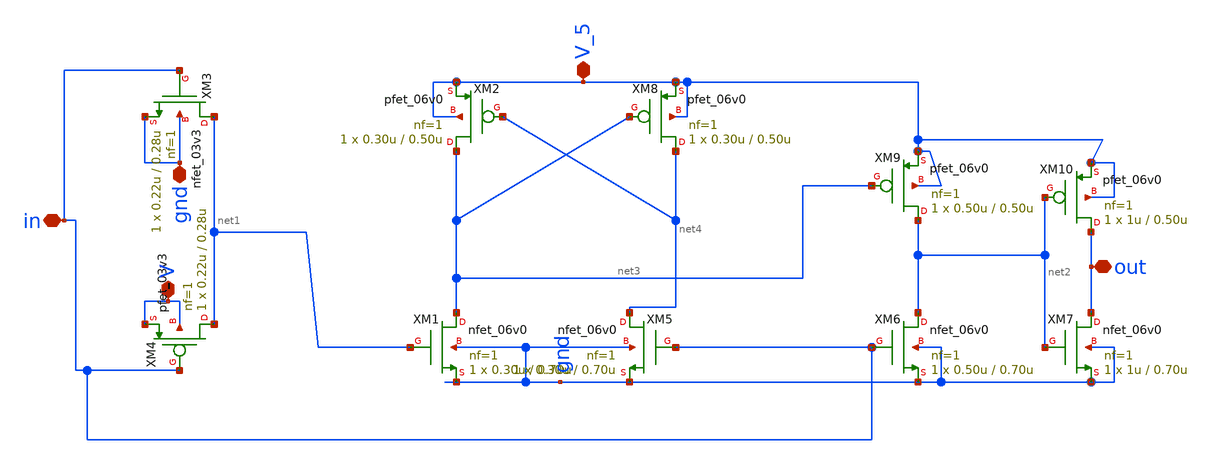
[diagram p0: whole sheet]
** sch_path: xschem/driver_5.sch
**.subckt driver_5 in out gnd V_5 V
*.iopin in
*.iopin out
*.iopin gnd
*.iopin V_5
*.iopin V
XM3 net1 in gnd gnd nfet_03v3 L=0.28u W=0.22u nf=1 ad='int((nf+1)/2) * W/nf * 0.18u' as='int((nf+2)/2) * W/nf * 0.18u'
+ pd='2*int((nf+1)/2) * (W/nf + 0.18u)' ps='2*int((nf+2)/2) * (W/nf + 0.18u)' nrd='0.18u / W' nrs='0.18u / W'
+ sa=0 sb=0 sd=0 m=1
XM4 net1 in V V pfet_03v3 L=0.28u W=0.22u nf=1 ad='int((nf+1)/2) * W/nf * 0.18u' as='int((nf+2)/2) * W/nf * 0.18u'
+ pd='2*int((nf+1)/2) * (W/nf + 0.18u)' ps='2*int((nf+2)/2) * (W/nf + 0.18u)' nrd='0.18u / W' nrs='0.18u / W'
+ sa=0 sb=0 sd=0 m=1
XM1 net3 net1 gnd gnd nfet_06v0 L=0.70u W=0.30u nf=1 ad='int((nf+1)/2) * W/nf * 0.18u' as='int((nf+2)/2) * W/nf * 0.18u'
+ pd='2*int((nf+1)/2) * (W/nf + 0.18u)' ps='2*int((nf+2)/2) * (W/nf + 0.18u)' nrd='0.18u / W' nrs='0.18u / W'
+ sa=0 sb=0 sd=0 m=1
XM2 net3 net4 V_5 V_5 pfet_06v0 L=0.50u W=0.30u nf=1 ad='int((nf+1)/2) * W/nf * 0.18u' as='int((nf+2)/2) * W/nf * 0.18u'
+ pd='2*int((nf+1)/2) * (W/nf + 0.18u)' ps='2*int((nf+2)/2) * (W/nf + 0.18u)' nrd='0.18u / W' nrs='0.18u / W'
+ sa=0 sb=0 sd=0 m=1
XM5 net4 in gnd gnd nfet_06v0 L=0.70u W=0.30u nf=1 ad='int((nf+1)/2) * W/nf * 0.18u' as='int((nf+2)/2) * W/nf * 0.18u'
+ pd='2*int((nf+1)/2) * (W/nf + 0.18u)' ps='2*int((nf+2)/2) * (W/nf + 0.18u)' nrd='0.18u / W' nrs='0.18u / W'
+ sa=0 sb=0 sd=0 m=1
XM6 net2 in gnd gnd nfet_06v0 L=0.70u W=0.50u nf=1 ad='int((nf+1)/2) * W/nf * 0.18u' as='int((nf+2)/2) * W/nf * 0.18u'
+ pd='2*int((nf+1)/2) * (W/nf + 0.18u)' ps='2*int((nf+2)/2) * (W/nf + 0.18u)' nrd='0.18u / W' nrs='0.18u / W'
+ sa=0 sb=0 sd=0 m=1
XM7 out net2 gnd gnd nfet_06v0 L=0.70u W=1u nf=1 ad='int((nf+1)/2) * W/nf * 0.18u' as='int((nf+2)/2) * W/nf * 0.18u'
+ pd='2*int((nf+1)/2) * (W/nf + 0.18u)' ps='2*int((nf+2)/2) * (W/nf + 0.18u)' nrd='0.18u / W' nrs='0.18u / W'
+ sa=0 sb=0 sd=0 m=1
XM8 net4 net3 V_5 V_5 pfet_06v0 L=0.50u W=0.30u nf=1 ad='int((nf+1)/2) * W/nf * 0.18u' as='int((nf+2)/2) * W/nf * 0.18u'
+ pd='2*int((nf+1)/2) * (W/nf + 0.18u)' ps='2*int((nf+2)/2) * (W/nf + 0.18u)' nrd='0.18u / W' nrs='0.18u / W'
+ sa=0 sb=0 sd=0 m=1
XM9 net2 net3 V_5 V_5 pfet_06v0 L=0.50u W=0.50u nf=1 ad='int((nf+1)/2) * W/nf * 0.18u' as='int((nf+2)/2) * W/nf * 0.18u'
+ pd='2*int((nf+1)/2) * (W/nf + 0.18u)' ps='2*int((nf+2)/2) * (W/nf + 0.18u)' nrd='0.18u / W' nrs='0.18u / W'
+ sa=0 sb=0 sd=0 m=1
XM10 out net2 V_5 V_5 pfet_06v0 L=0.50u W=1u nf=1 ad='int((nf+1)/2) * W/nf * 0.18u' as='int((nf+2)/2) * W/nf * 0.18u'
+ pd='2*int((nf+1)/2) * (W/nf + 0.18u)' ps='2*int((nf+2)/2) * (W/nf + 0.18u)' nrd='0.18u / W' nrs='0.18u / W'
+ sa=0 sb=0 sd=0 m=1
**.ends
.end
